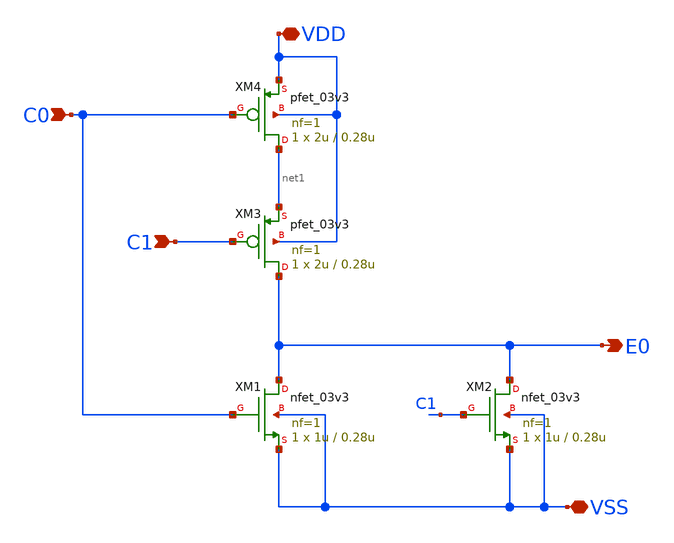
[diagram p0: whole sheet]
** sch_path: designs/digital/schematic/nor.sch
**.subckt nor VDD VSS C0 C1 E0
*.iopin VDD
*.iopin VSS
*.ipin C0
*.ipin C1
*.opin E0
XM1 E0 C0 VSS VSS nfet_03v3 L=0.28u W=1u nf=1 ad='int((nf+1)/2) * W/nf * 0.18u' as='int((nf+2)/2) * W/nf * 0.18u'
+ pd='2*int((nf+1)/2) * (W/nf + 0.18u)' ps='2*int((nf+2)/2) * (W/nf + 0.18u)' nrd='0.18u / W' nrs='0.18u / W'
+ sa=0 sb=0 sd=0 m=1
XM2 E0 C1 VSS VSS nfet_03v3 L=0.28u W=1u nf=1 ad='int((nf+1)/2) * W/nf * 0.18u' as='int((nf+2)/2) * W/nf * 0.18u'
+ pd='2*int((nf+1)/2) * (W/nf + 0.18u)' ps='2*int((nf+2)/2) * (W/nf + 0.18u)' nrd='0.18u / W' nrs='0.18u / W'
+ sa=0 sb=0 sd=0 m=1
XM3 E0 C1 net1 VDD pfet_03v3 L=0.28u W=2u nf=1 ad='int((nf+1)/2) * W/nf * 0.18u' as='int((nf+2)/2) * W/nf * 0.18u'
+ pd='2*int((nf+1)/2) * (W/nf + 0.18u)' ps='2*int((nf+2)/2) * (W/nf + 0.18u)' nrd='0.18u / W' nrs='0.18u / W'
+ sa=0 sb=0 sd=0 m=1
XM4 net1 C0 VDD VDD pfet_03v3 L=0.28u W=2u nf=1 ad='int((nf+1)/2) * W/nf * 0.18u' as='int((nf+2)/2) * W/nf * 0.18u'
+ pd='2*int((nf+1)/2) * (W/nf + 0.18u)' ps='2*int((nf+2)/2) * (W/nf + 0.18u)' nrd='0.18u / W' nrs='0.18u / W'
+ sa=0 sb=0 sd=0 m=1
**.ends
.end
